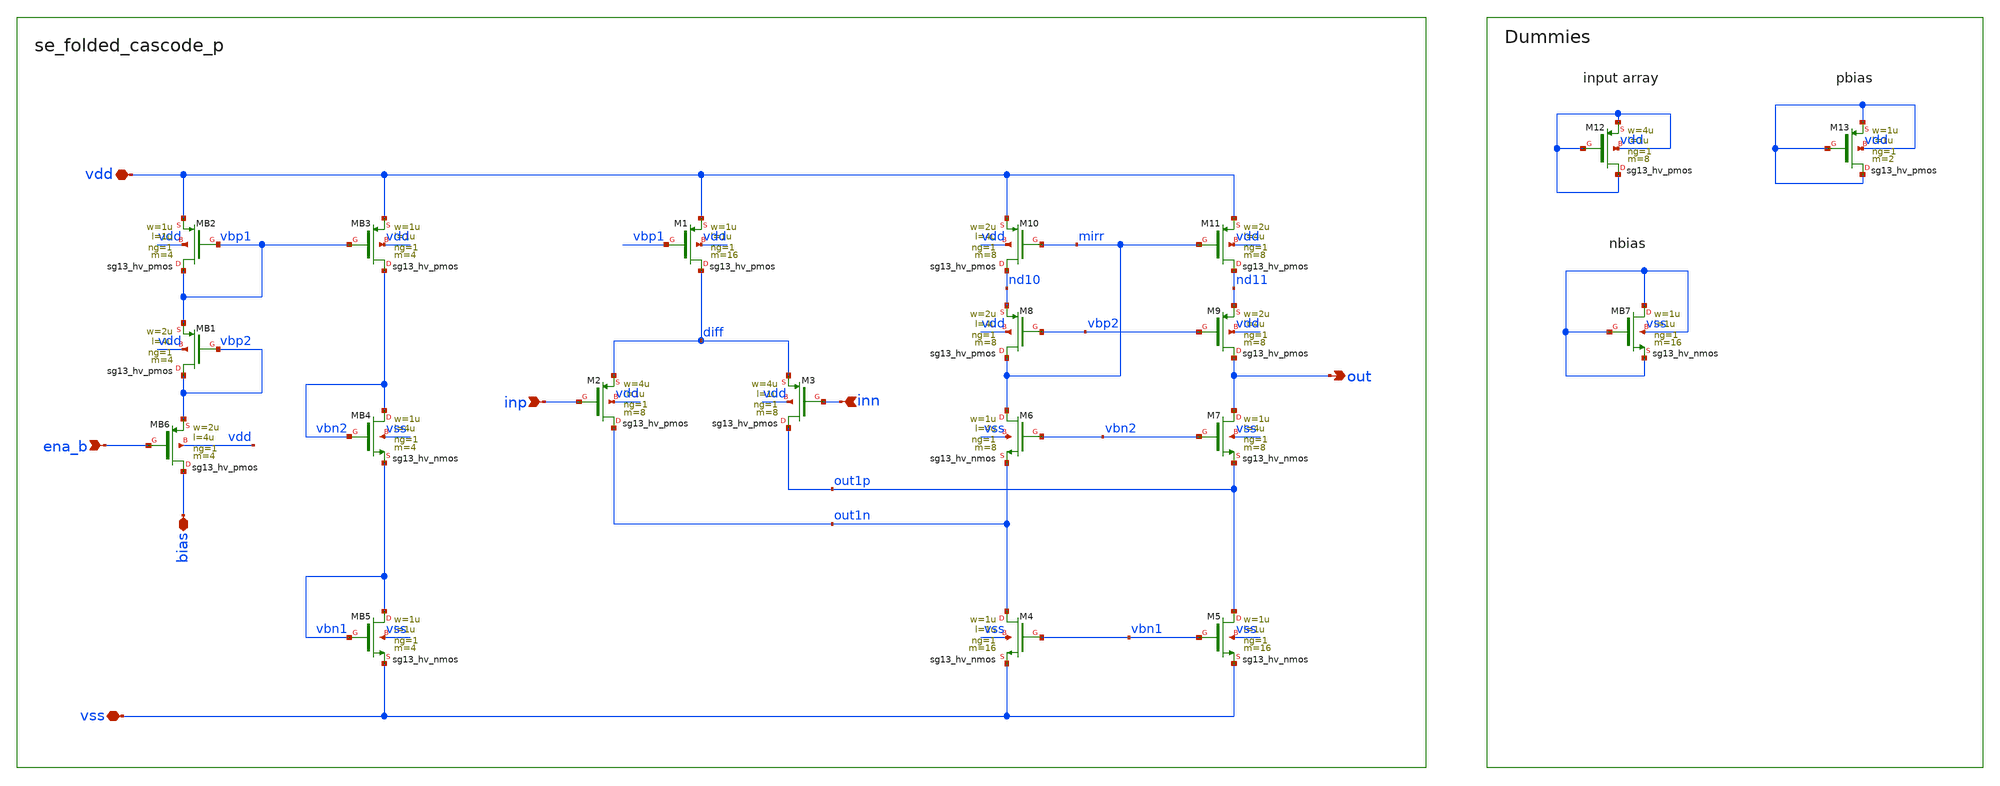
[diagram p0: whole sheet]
** sch_path: xschem/se_folded_cascode_p.sch
**.subckt se_folded_cascode_p inn inp out bias vdd vss ena_b
*.ipin inn
*.ipin inp
*.opin out
*.iopin bias
*.iopin vdd
*.iopin vss
*.ipin ena_b
XM3 out1p inn diff vdd sg13_hv_pmos w=4u l=1u ng=1 m=8 mm_ok=1
XM2 out1n inp diff vdd sg13_hv_pmos w=4u l=1u ng=1 m=8 mm_ok=1
XM1 diff vbp1 vdd vdd sg13_hv_pmos w=1u l=1u ng=1 m=16 mm_ok=1
XM4 out1n vbn1 vss vss sg13_hv_nmos w=1u l=1u ng=1 m=16 mm_ok=1
XM5 out1p vbn1 vss vss sg13_hv_nmos w=1u l=1u ng=1 m=16 mm_ok=1
XM6 mirr vbn2 out1n vss sg13_hv_nmos w=1u l=4u ng=1 m=8 mm_ok=1
XM7 out vbn2 out1p vss sg13_hv_nmos w=1u l=4u ng=1 m=8 mm_ok=1
XM8 mirr vbp2 nd10 vdd sg13_hv_pmos w=2u l=4u ng=1 m=8 mm_ok=1
XM9 out vbp2 nd11 vdd sg13_hv_pmos w=2u l=4u ng=1 m=8 mm_ok=1
XM10 nd10 mirr vdd vdd sg13_hv_pmos w=2u l=4u ng=1 m=8 mm_ok=1
XM11 nd11 mirr vdd vdd sg13_hv_pmos w=2u l=4u ng=1 m=8 mm_ok=1
XMB1 vbp2 vbp2 vbp1 vdd sg13_hv_pmos w=2u l=4u ng=1 m=4 mm_ok=1
XMB2 vbp1 vbp1 vdd vdd sg13_hv_pmos w=1u l=1u ng=1 m=4 mm_ok=1
XMB3 vbn2 vbp1 vdd vdd sg13_hv_pmos w=1u l=1u ng=1 m=4 mm_ok=1
XMB4 vbn2 vbn2 vbn1 vss sg13_hv_nmos w=1u l=4u ng=1 m=4 mm_ok=1
XMB5 vbn1 vbn1 vss vss sg13_hv_nmos w=1u l=1u ng=1 m=4 mm_ok=1
XMB6 bias ena_b vbp2 vdd sg13_hv_pmos w=2u l=4u ng=1 m=4 mm_ok=1
XM12 vdd vdd vdd vdd sg13_hv_pmos w=4u l=1u ng=1 m=8 mm_ok=1
XM13 vdd vdd vdd vdd sg13_hv_pmos w=1u l=1u ng=1 m=2 mm_ok=1
XMB7 vss vss vss vss sg13_hv_nmos w=1u l=1u ng=1 m=16 mm_ok=1
**.ends
.end
